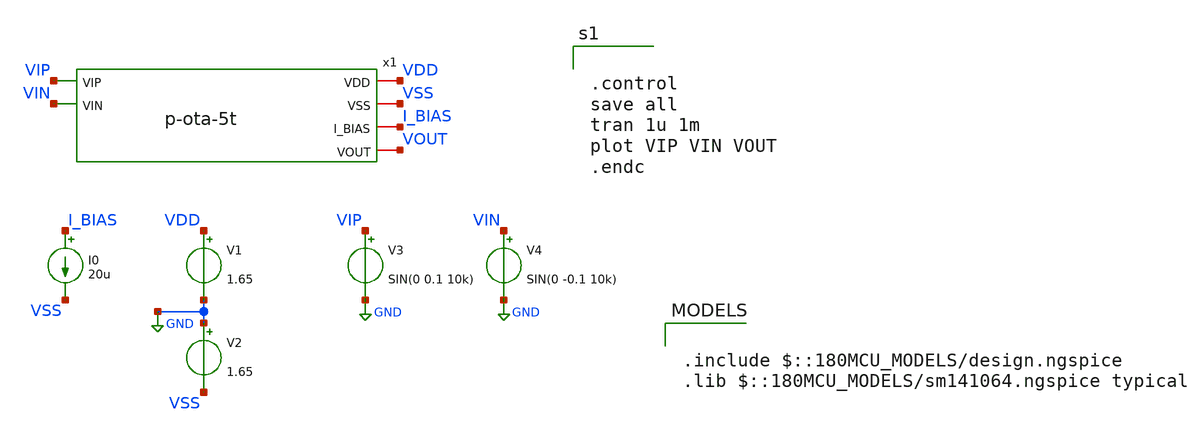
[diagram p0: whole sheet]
** sch_path: designs/libs/tb_analog/tb_p-ota/tb_p-ota-5t.sch
**.subckt tb_p-ota-5t
x1 VDD VSS I_BIAS VIP VIN VOUT p-ota-5t
V1 VDD GND 1.65
V2 GND VSS 1.65
V3 VIP GND SIN(0 0.1 10k)
V4 VIN GND SIN(0 -0.1 10k)
I0 I_BIAS VSS 20u
**** begin user architecture code

.include $::180MCU_MODELS/design.ngspice
.lib $::180MCU_MODELS/sm141064.ngspice typical



.control
save all
tran 1u 1m
plot VIP VIN VOUT
.endc


**** end user architecture code
**.ends

* expanding   symbol:  sscs-chipathon2025-LNA/designs/libs/core_analog/p-ota/p-ota-5t.sym # of
*+ pins=6
** sym_path: designs/libs/core_analog/p-ota/p-ota-5t.sym
** sch_path: designs/libs/core_analog/p-ota/p-ota-5t.sch
.subckt p-ota-5t VDD VSS I_BIAS VIP VIN VOUT
*.iopin VDD
*.iopin VSS
*.iopin I_BIAS
*.ipin VIP
*.ipin VIN
*.iopin VOUT
XM1 net2 I_BIAS VDD VDD pfet_03v3 L=0.5u W=2u nf=1 ad='int((nf+1)/2) * W/nf * 0.18u' as='int((nf+2)/2) * W/nf * 0.18u'
+ pd='2*int((nf+1)/2) * (W/nf + 0.18u)' ps='2*int((nf+2)/2) * (W/nf + 0.18u)' nrd='0.18u / W' nrs='0.18u / W'
+ sa=0 sb=0 sd=0 m=1
XM2 net1 VIP net2 VDD pfet_03v3 L=0.5u W=5u nf=1 ad='int((nf+1)/2) * W/nf * 0.18u' as='int((nf+2)/2) * W/nf * 0.18u'
+ pd='2*int((nf+1)/2) * (W/nf + 0.18u)' ps='2*int((nf+2)/2) * (W/nf + 0.18u)' nrd='0.18u / W' nrs='0.18u / W'
+ sa=0 sb=0 sd=0 m=1
XM3 VOUT VIN net2 VDD pfet_03v3 L=0.5u W=5u nf=1 ad='int((nf+1)/2) * W/nf * 0.18u' as='int((nf+2)/2) * W/nf * 0.18u'
+ pd='2*int((nf+1)/2) * (W/nf + 0.18u)' ps='2*int((nf+2)/2) * (W/nf + 0.18u)' nrd='0.18u / W' nrs='0.18u / W'
+ sa=0 sb=0 sd=0 m=1
XM4 I_BIAS I_BIAS VDD VDD pfet_03v3 L=0.5u W=10u nf=1 ad='int((nf+1)/2) * W/nf * 0.18u' as='int((nf+2)/2) * W/nf * 0.18u'
+ pd='2*int((nf+1)/2) * (W/nf + 0.18u)' ps='2*int((nf+2)/2) * (W/nf + 0.18u)' nrd='0.18u / W' nrs='0.18u / W'
+ sa=0 sb=0 sd=0 m=1
XM5 VOUT net1 VSS VSS nfet_03v3 L=0.5u W=2u nf=1 ad='int((nf+1)/2) * W/nf * 0.18u' as='int((nf+2)/2) * W/nf * 0.18u'
+ pd='2*int((nf+1)/2) * (W/nf + 0.18u)' ps='2*int((nf+2)/2) * (W/nf + 0.18u)' nrd='0.18u / W' nrs='0.18u / W'
+ sa=0 sb=0 sd=0 m=1
XM6 net1 net1 VSS VSS nfet_03v3 L=0.5u W=2u nf=1 ad='int((nf+1)/2) * W/nf * 0.18u' as='int((nf+2)/2) * W/nf * 0.18u'
+ pd='2*int((nf+1)/2) * (W/nf + 0.18u)' ps='2*int((nf+2)/2) * (W/nf + 0.18u)' nrd='0.18u / W' nrs='0.18u / W'
+ sa=0 sb=0 sd=0 m=1
.ends

.GLOBAL GND
.end
